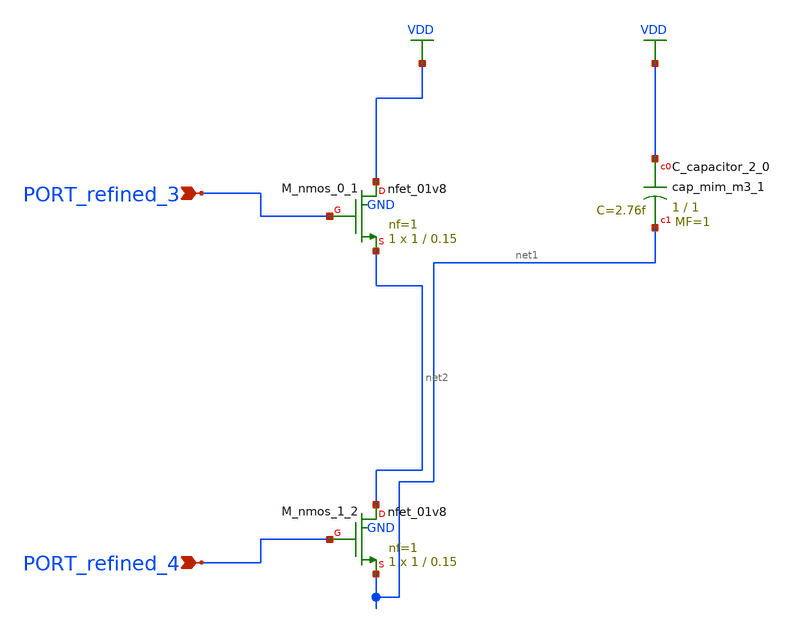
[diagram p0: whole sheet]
** sch_path: schematics/AMSNet/181.sch
**.subckt 181 PORT_refined_3 PORT_refined_4
*.ipin PORT_refined_3
*.ipin PORT_refined_4
XC_capacitor_2_0 VDD net1 sky130_fd_pr__cap_mim_m3_1 W=1 L=1 MF=1 m=1
XM_nmos_0_1 VDD PORT_refined_3 net2 GND sky130_fd_pr__nfet_01v8 L=0.15 W=1 nf=1 ad='int((1 + 1)/2) * 1 / 1 * 0.29'
+ as='int((1 + 2)/2) * 1 / 1 * 0.29' pd='2*int((1 + 1)/2) * (1 / 1 + 0.29)' ps='2*int((1 + 2)/2) * (1 / 1 + 0.29)'
+ nrd='0.29 / 1 ' nrs='0.29 / 1 ' sa=0 sb=0 sd=0 mult=1 m=1
XM_nmos_1_2 net2 PORT_refined_4 net1 GND sky130_fd_pr__nfet_01v8 L=0.15 W=1 nf=1 ad='int((1 + 1)/2) * 1 / 1 * 0.29'
+ as='int((1 + 2)/2) * 1 / 1 * 0.29' pd='2*int((1 + 1)/2) * (1 / 1 + 0.29)' ps='2*int((1 + 2)/2) * (1 / 1 + 0.29)'
+ nrd='0.29 / 1 ' nrs='0.29 / 1 ' sa=0 sb=0 sd=0 mult=1 m=1
**.ends
.GLOBAL VDD
.end
